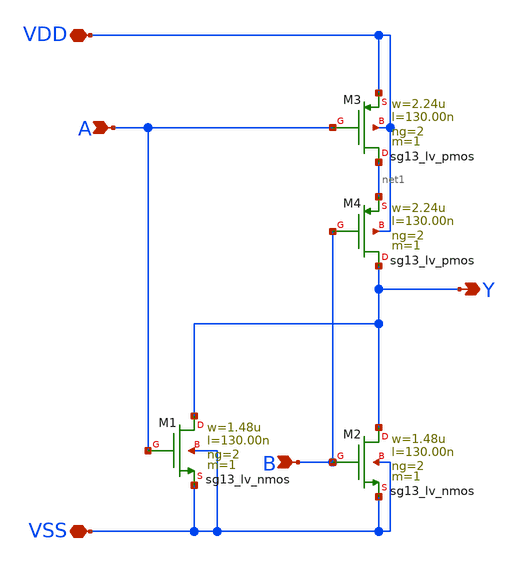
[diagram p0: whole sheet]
** sch_path: ihp-sg13g2/libs.tech/xschem/sg13g2_stdcells/sg13g2_nor2_2.sch
* Copyright 2023 IHP PDK Authors
* Licensed under the Apache License, Version 2.0 (the "License");
* you may not use this file except in compliance with the License.
* You may obtain a copy of the License at
* https://www.apache.org/licenses/LICENSE-2.0
* Unless required by applicable law or agreed to in writing, software
* distributed under the License is distributed on an "AS IS" BASIS,
* WITHOUT WARRANTIES OR CONDITIONS OF ANY KIND, either express or implied.
* See the License for the specific language governing permissions and
* limitations under the License.
**.subckt sg13g2_nor2_2 Y B A VDD VSS
*.opin Y
*.ipin B
*.ipin A
*.iopin VDD
*.iopin VSS
XM1 Y A VSS VSS sg13_lv_nmos w=1.48u l=130.00n ng=2 m=1 mm_ok=1
XM2 Y B VSS VSS sg13_lv_nmos w=1.48u l=130.00n ng=2 m=1 mm_ok=1
XM3 net1 A VDD VDD sg13_lv_pmos w=2.24u l=130.00n ng=2 m=1 mm_ok=1
XM4 Y B net1 VDD sg13_lv_pmos w=2.24u l=130.00n ng=2 m=1 mm_ok=1
**.ends
.end
